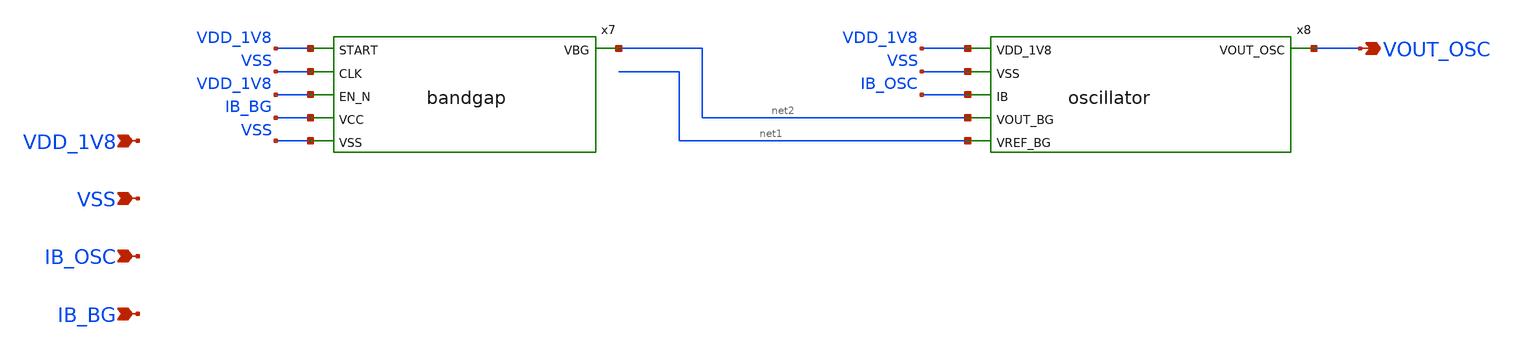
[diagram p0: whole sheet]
** sch_path: design/LELO_GR01_SKY130A/oscillator_tb.sch
**.subckt oscillator_tb VSS VDD_1V8 IB_OSC IB_BG VOUT_OSC
*.ipin VSS
*.ipin VDD_1V8
*.ipin IB_OSC
*.ipin IB_BG
*.opin VOUT_OSC
x7 VDD_1V8 VSS VDD_1V8 net2 IB_BG VSS bandgap
x8 VOUT_OSC VDD_1V8 VSS IB_OSC net2 net1 oscillator
**.ends
.end
